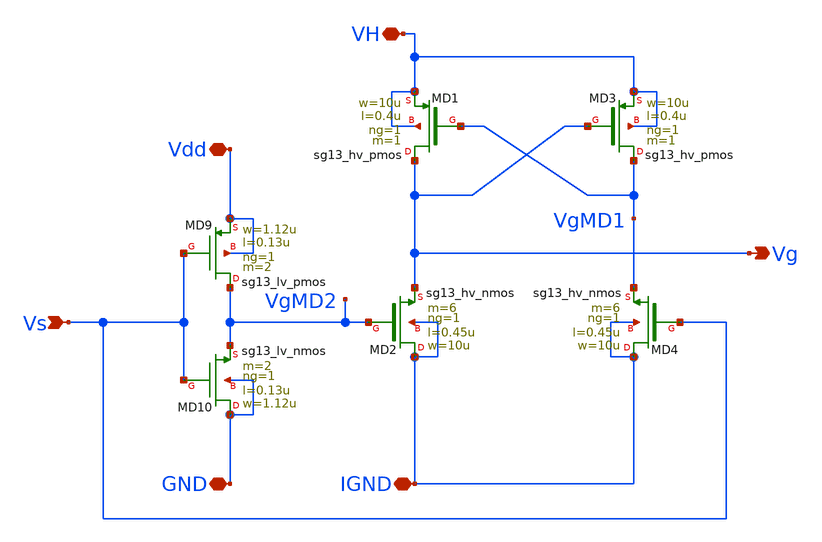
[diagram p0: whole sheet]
** sch_path: ChipUSM_AnalogTrack24/LSLH/LSLH_vto1p1.sch
**.subckt LSLH_vto1p1 VH Vdd Vs Vg GND IGND
*.iopin VH
*.iopin Vdd
*.ipin Vs
*.opin Vg
*.iopin GND
*.iopin IGND
XMD9 VgMD2 Vs Vdd Vdd sg13_lv_pmos w=1.12u l=0.13u ng=1 m=2 mm_ok=1
XMD10 GND Vs VgMD2 GND sg13_lv_nmos w=1.12u l=0.13u ng=1 m=2 mm_ok=1
XMD1 Vg VgMD1 VH VH sg13_hv_pmos w=10u l=0.4u ng=1 m=1 mm_ok=1
XMD3 VgMD1 Vg VH VH sg13_hv_pmos w=10u l=0.4u ng=1 m=1 mm_ok=1
XMD2 IGND VgMD2 Vg IGND sg13_hv_nmos w=10u l=0.45u ng=1 m=6 mm_ok=1
XMD4 IGND Vs VgMD1 IGND sg13_hv_nmos w=10u l=0.45u ng=1 m=6 mm_ok=1
**.ends
.end
